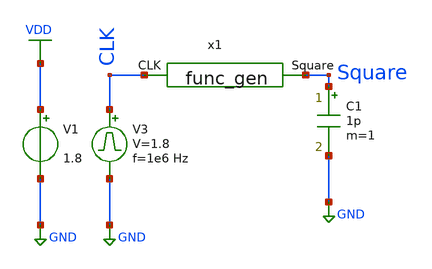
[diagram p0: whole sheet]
** sch_path: library/xschem/func_gen_tb.sch
**.subckt func_gen_tb
V1 VDD GND 1.8
C1 Square GND 1p m=1
V3 CLK GND pulse 0 1.8 '0.495/ 1e6 ' '0.01/1e6 ' '0.01/1e6 ' '0.49/1e6 ' '1/1e6 '
x1 Square CLK func_gen
**** begin user architecture code


.control
save all
tran 1n 260u
plot V(CLK) V(Square)+2
.endc


** opencircuitdesign pdks install
.lib $::SKYWATER_MODELS/sky130.lib.spice tt


**** end user architecture code
**.ends
.GLOBAL VDD
.GLOBAL GND
.end
